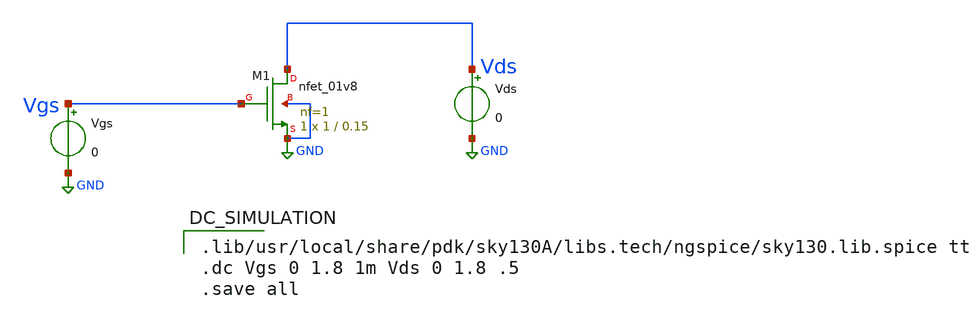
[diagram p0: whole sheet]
** sch_path: Xschem-Files/dc_sweep.sch
**.subckt dc_sweep
XM1 Vds Vgs GND GND sky130_fd_pr__nfet_01v8 L=0.15 W=1 nf=1 ad='int((1 + 1)/2) * 1 / 1 * 0.29' as='int((1 + 2)/2) * 1 / 1 * 0.29'
+ pd='2*int((1 + 1)/2) * (1 / 1 + 0.29)' ps='2*int((1 + 2)/2) * (1 / 1 + 0.29)' nrd='0.29 / 1 ' nrs='0.29 / 1 '
+ sa=0 sb=0 sd=0 mult=1 m=1
Vds Vds GND 0
Vgs Vgs GND 0
**** begin user architecture code

.lib/usr/local/share/pdk/sky130A/libs.tech/ngspice/sky130.lib.spice tt
.dc Vgs 0 1.8 1m Vds 0 1.8 .5
.save all

**** end user architecture code
**.ends
.GLOBAL GND
.end
